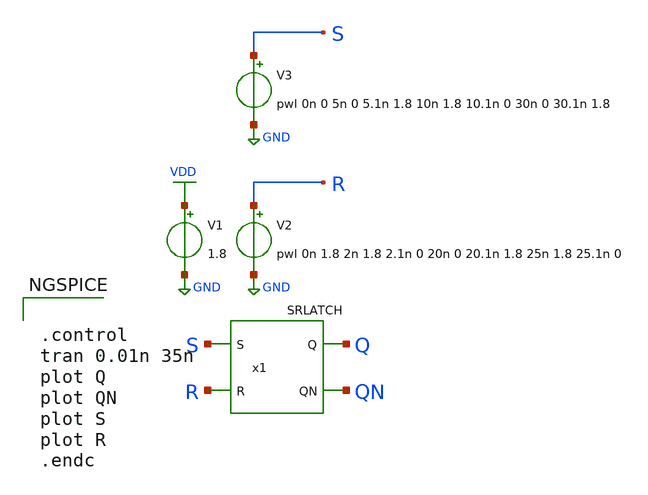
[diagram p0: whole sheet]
** sch_path: lib/xschem/test_SRLATCH.sch
**.subckt test_SRLATCH
V2 R GND pwl 0n 1.8 2n 1.8 2.1n 0 20n 0 20.1n 1.8 25n 1.8 25.1n 0
V1 VDD GND 1.8
V3 S GND pwl 0n 0 5n 0 5.1n 1.8 10n 1.8 10.1n 0 30n 0 30.1n 1.8
x1 Q QN S R VDD GND SRLATCH
**** begin user architecture code

.lib $::SKYWATER_MODELS/sky130.lib.spice tt


**** end user architecture code
**.ends

* expanding   symbol:  SRLATCH.sym # of pins=4
** sym_path: lib/xschem/SRLATCH.sym
** sch_path: lib/xschem/SRLATCH.sch
.subckt SRLATCH Q QN S R VCCPIN VSSPIN
*.ipin S
*.ipin R
*.opin QN
*.opin Q
x1 Q QN R NOR2X1
x2 QN S Q NOR2X1
.ends


* expanding   symbol:  NOR2X1.sym # of pins=3
** sym_path: lib/xschem/NOR2X1.sym
** sch_path: lib/xschem/NOR2X1.sch
.subckt NOR2X1 Y A B
*.opin Y
*.ipin A
*.ipin B
XM1 Y A VSS VSS sky130_fd_pr__nfet_01v8 L=0.15 W=3 nf=1 ad='int((nf+1)/2) * W/nf * 0.29' as='int((nf+2)/2) * W/nf * 0.29'
+ pd='2*int((nf+1)/2) * (W/nf + 0.29)' ps='2*int((nf+2)/2) * (W/nf + 0.29)' nrd='0.29 / W' nrs='0.29 / W'
+ sa=0 sb=0 sd=0 mult=1 m=1
XM2 net1 A VDD VDD sky130_fd_pr__pfet_01v8 L=0.15 W=2 nf=1 ad='int((nf+1)/2) * W/nf * 0.29' as='int((nf+2)/2) * W/nf * 0.29'
+ pd='2*int((nf+1)/2) * (W/nf + 0.29)' ps='2*int((nf+2)/2) * (W/nf + 0.29)' nrd='0.29 / W' nrs='0.29 / W'
+ sa=0 sb=0 sd=0 mult=2 m=2
XM3 Y B VSS VSS sky130_fd_pr__nfet_01v8 L=0.15 W=3 nf=1 ad='int((nf+1)/2) * W/nf * 0.29' as='int((nf+2)/2) * W/nf * 0.29'
+ pd='2*int((nf+1)/2) * (W/nf + 0.29)' ps='2*int((nf+2)/2) * (W/nf + 0.29)' nrd='0.29 / W' nrs='0.29 / W'
+ sa=0 sb=0 sd=0 mult=1 m=1
XM5 Y B net1 VDD sky130_fd_pr__pfet_01v8 L=0.15 W=2 nf=1 ad='int((nf+1)/2) * W/nf * 0.29' as='int((nf+2)/2) * W/nf * 0.29'
+ pd='2*int((nf+1)/2) * (W/nf + 0.29)' ps='2*int((nf+2)/2) * (W/nf + 0.29)' nrd='0.29 / W' nrs='0.29 / W'
+ sa=0 sb=0 sd=0 mult=2 m=2
.ends

.GLOBAL VDD
.GLOBAL GND
**** begin user architecture code


.control
tran 0.01n 35n
plot Q
plot QN
plot S
plot R
.endc


**** end user architecture code
.end
